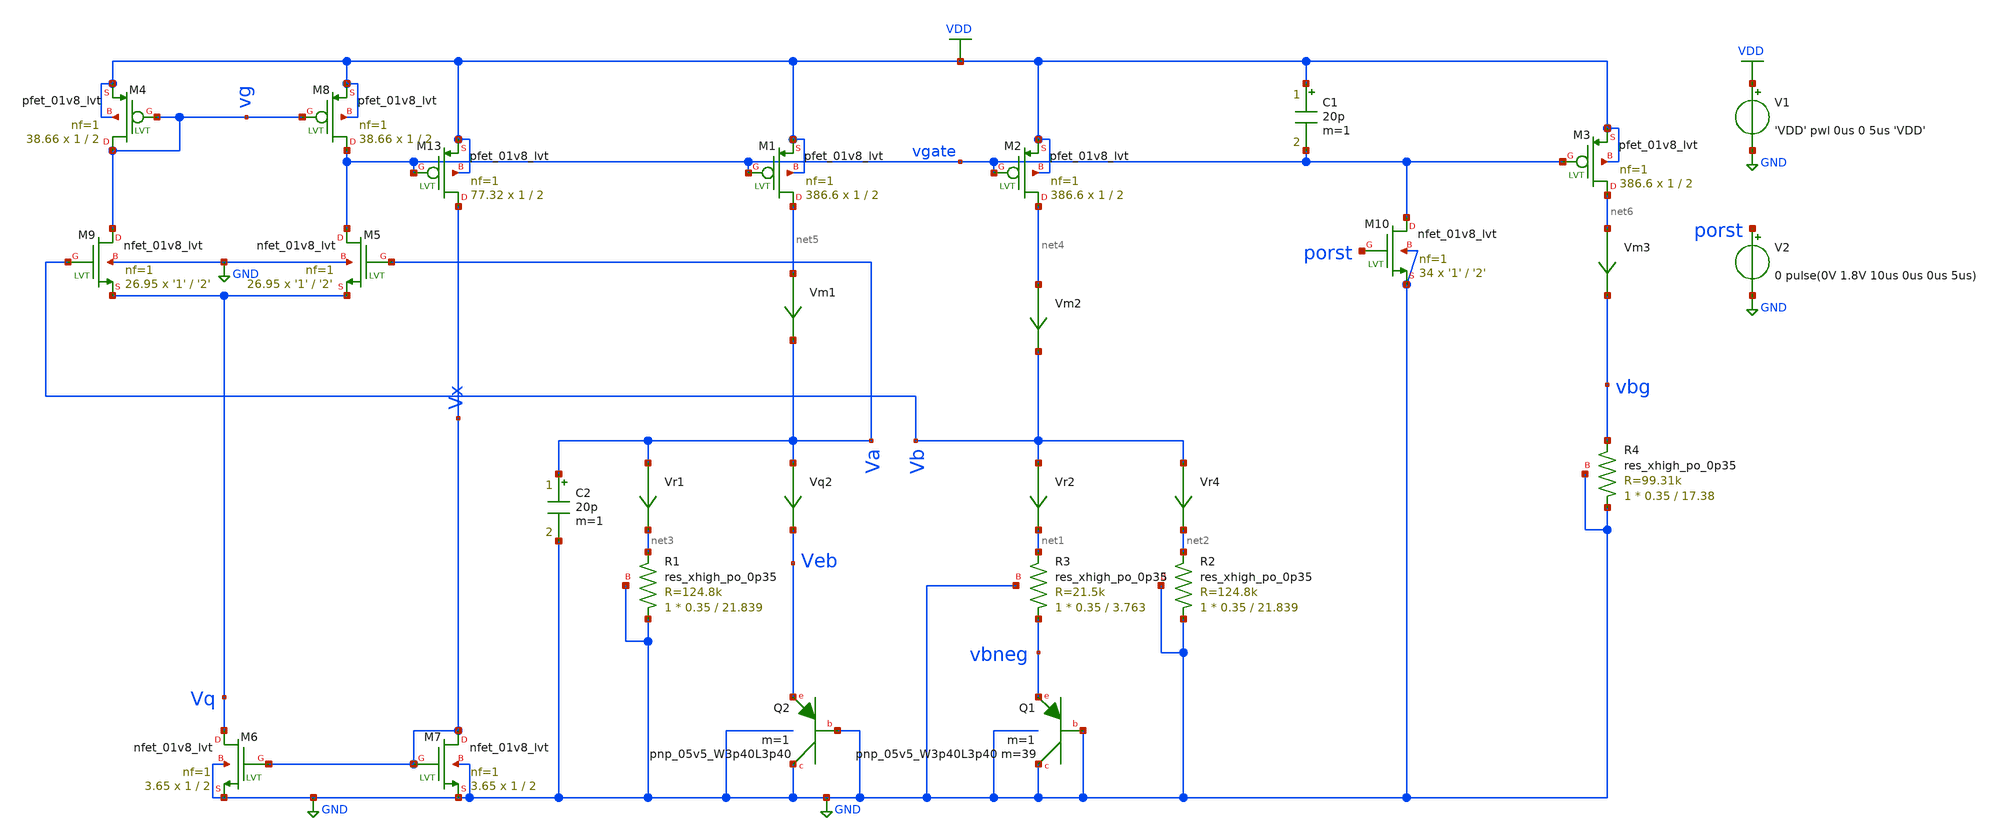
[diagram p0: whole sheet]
** sch_path: VLSI23/bandgap_sky130_v1/tests/tran/tsmc_bandgap_real_tran.sch
**.subckt tsmc_bandgap_real_tran
V1 VDD GND 'VDD' pwl 0us 0 5us 'VDD'
XQ2 GND GND Veb sky130_fd_pr__pnp_05v5_W3p40L3p40 m=1
Vr4 Vb net2 0
.save i(vr4)
Vr2 Vb net1 0
.save i(vr2)
Vm1 net5 Va 0
.save i(vm1)
Vm2 net4 Vb 0
.save i(vm2)
Vm3 net6 vbg 0
.save i(vm3)
Vr1 Va net3 0
.save i(vr1)
Vq2 Va Veb 0
.save i(vq2)
XQ1 GND GND vbneg sky130_fd_pr__pnp_05v5_W3p40L3p40 m=39 m=1
XM5 vgate Va Vq GND sky130_fd_pr__nfet_01v8_lvt L='2' W='1' nf=1 ad='int((nf+1)/2) * W/nf * 0.29' as='int((nf+2)/2) * W/nf * 0.29'
+ pd='2*int((nf+1)/2) * (W/nf + 0.29)' ps='2*int((nf+2)/2) * (W/nf + 0.29)' nrd='0.29 / W' nrs='0.29 / W'
+ sa=0 sb=0 sd=0 mult=26.95 m=26.95
XM6 Vq Vx GND GND sky130_fd_pr__nfet_01v8_lvt L=2 W=1 nf=1 ad='int((nf+1)/2) * W/nf * 0.29' as='int((nf+2)/2) * W/nf * 0.29'
+ pd='2*int((nf+1)/2) * (W/nf + 0.29)' ps='2*int((nf+2)/2) * (W/nf + 0.29)' nrd='0.29 / W' nrs='0.29 / W'
+ sa=0 sb=0 sd=0 mult=3.65 m=3.65
XM9 vg Vb Vq GND sky130_fd_pr__nfet_01v8_lvt L='2' W='1' nf=1 ad='int((nf+1)/2) * W/nf * 0.29' as='int((nf+2)/2) * W/nf * 0.29'
+ pd='2*int((nf+1)/2) * (W/nf + 0.29)' ps='2*int((nf+2)/2) * (W/nf + 0.29)' nrd='0.29 / W' nrs='0.29 / W'
+ sa=0 sb=0 sd=0 mult=26.95 m=26.95
XM7 Vx Vx GND GND sky130_fd_pr__nfet_01v8_lvt L=2 W=1 nf=1 ad='int((nf+1)/2) * W/nf * 0.29' as='int((nf+2)/2) * W/nf * 0.29'
+ pd='2*int((nf+1)/2) * (W/nf + 0.29)' ps='2*int((nf+2)/2) * (W/nf + 0.29)' nrd='0.29 / W' nrs='0.29 / W'
+ sa=0 sb=0 sd=0 mult=3.65 m=3.65
XM13 Vx vgate VDD VDD sky130_fd_pr__pfet_01v8_lvt L=2 W=1 nf=1 ad='int((nf+1)/2) * W/nf * 0.29' as='int((nf+2)/2) * W/nf * 0.29'
+ pd='2*int((nf+1)/2) * (W/nf + 0.29)' ps='2*int((nf+2)/2) * (W/nf + 0.29)' nrd='0.29 / W' nrs='0.29 / W'
+ sa=0 sb=0 sd=0 mult=77.32 m=77.32
XM1 net5 vgate VDD VDD sky130_fd_pr__pfet_01v8_lvt L=2 W=1 nf=1 ad='int((nf+1)/2) * W/nf * 0.29' as='int((nf+2)/2) * W/nf * 0.29'
+ pd='2*int((nf+1)/2) * (W/nf + 0.29)' ps='2*int((nf+2)/2) * (W/nf + 0.29)' nrd='0.29 / W' nrs='0.29 / W'
+ sa=0 sb=0 sd=0 mult=386.6 m=386.6
XM2 net4 vgate VDD VDD sky130_fd_pr__pfet_01v8_lvt L=2 W=1 nf=1 ad='int((nf+1)/2) * W/nf * 0.29' as='int((nf+2)/2) * W/nf * 0.29'
+ pd='2*int((nf+1)/2) * (W/nf + 0.29)' ps='2*int((nf+2)/2) * (W/nf + 0.29)' nrd='0.29 / W' nrs='0.29 / W'
+ sa=0 sb=0 sd=0 mult=386.6 m=386.6
XM3 net6 vgate VDD VDD sky130_fd_pr__pfet_01v8_lvt L=2 W=1 nf=1 ad='int((nf+1)/2) * W/nf * 0.29' as='int((nf+2)/2) * W/nf * 0.29'
+ pd='2*int((nf+1)/2) * (W/nf + 0.29)' ps='2*int((nf+2)/2) * (W/nf + 0.29)' nrd='0.29 / W' nrs='0.29 / W'
+ sa=0 sb=0 sd=0 mult=386.6 m=386.6
XR1 GND net3 GND sky130_fd_pr__res_xhigh_po_0p35 L=21.839 mult=1 m=1
XR2 GND net2 GND sky130_fd_pr__res_xhigh_po_0p35 L=21.839 mult=1 m=1
XR3 vbneg net1 GND sky130_fd_pr__res_xhigh_po_0p35 L=3.763 mult=1 m=1
XR4 GND vbg GND sky130_fd_pr__res_xhigh_po_0p35 L=17.38 mult=1 m=1
XM4 vg vg VDD VDD sky130_fd_pr__pfet_01v8_lvt L=2 W=1 nf=1 ad='int((nf+1)/2) * W/nf * 0.29' as='int((nf+2)/2) * W/nf * 0.29'
+ pd='2*int((nf+1)/2) * (W/nf + 0.29)' ps='2*int((nf+2)/2) * (W/nf + 0.29)' nrd='0.29 / W' nrs='0.29 / W'
+ sa=0 sb=0 sd=0 mult=38.66 m=38.66
XM8 vgate vg VDD VDD sky130_fd_pr__pfet_01v8_lvt L=2 W=1 nf=1 ad='int((nf+1)/2) * W/nf * 0.29' as='int((nf+2)/2) * W/nf * 0.29'
+ pd='2*int((nf+1)/2) * (W/nf + 0.29)' ps='2*int((nf+2)/2) * (W/nf + 0.29)' nrd='0.29 / W' nrs='0.29 / W'
+ sa=0 sb=0 sd=0 mult=38.66 m=38.66
XM10 vgate porst GND GND sky130_fd_pr__nfet_01v8_lvt L='2' W='1' nf=1 ad='int((nf+1)/2) * W/nf * 0.29'
+ as='int((nf+2)/2) * W/nf * 0.29' pd='2*int((nf+1)/2) * (W/nf + 0.29)' ps='2*int((nf+2)/2) * (W/nf + 0.29)'
+ nrd='0.29 / W' nrs='0.29 / W' sa=0 sb=0 sd=0 mult=34 m=34
V2 porst GND 0 pulse(0V 1.8V 10us 0us 0us 5us)
C1 VDD vgate 20p m=1
C2 Va GND 20p m=1
**** begin user architecture code


.option savecurrents
.param R3val='22.187k'
.param alpha='1'
.param R2R3ratio='5.6555038*alpha'
.param R2val='R3val*R2R3ratio'
.param R4R2ratio='0.79694273'
.param R4val='R2val*R4R2ratio
.param VDD=1.8
.control
save all  @m.xm1.msky130_fd_pr__pfet_01v8_lvt[gm]  @m.xm2.msky130_fd_pr__pfet_01v8_lvt[gm]  @m.xm3.msky130_fd_pr__pfet_01v8_lvt[gm]  @m.xm4.msky130_fd_pr__pfet_01v8_lvt[gm]  @m.xm5.msky130_fd_pr__nfet_01v8_lvt[gm]  @m.xm6.msky130_fd_pr__nfet_01v8_lvt[gm]  @m.xm7.msky130_fd_pr__nfet_01v8_lvt[gm]  @m.xm8.msky130_fd_pr__pfet_01v8_lvt[gm]  @m.xm9.msky130_fd_pr__nfet_01v8_lvt[gm]  @m.xm13.msky130_fd_pr__pfet_01v8_lvt[gm]

option temp=27
tran 0.1n 20u
option temp=0
tran 0.1n 20u
option temp=70
tran 0.1n 20u
write ./sims/tsmc_bandgap_real_70degc_vbg.raw vbg
setplot tran2
write ./sims/tsmc_bandgap_real_0degc_vbg.raw vbg
setplot tran1
write ./sims/tsmc_bandgap_real_27degc_vbg.raw vbg
unset askquit
quit
.endc



** opencircuitdesign pdks install
.lib $::SKYWATER_MODELS/sky130.lib.spice tt


**** end user architecture code
**.ends
.GLOBAL VDD
.GLOBAL GND
.end
